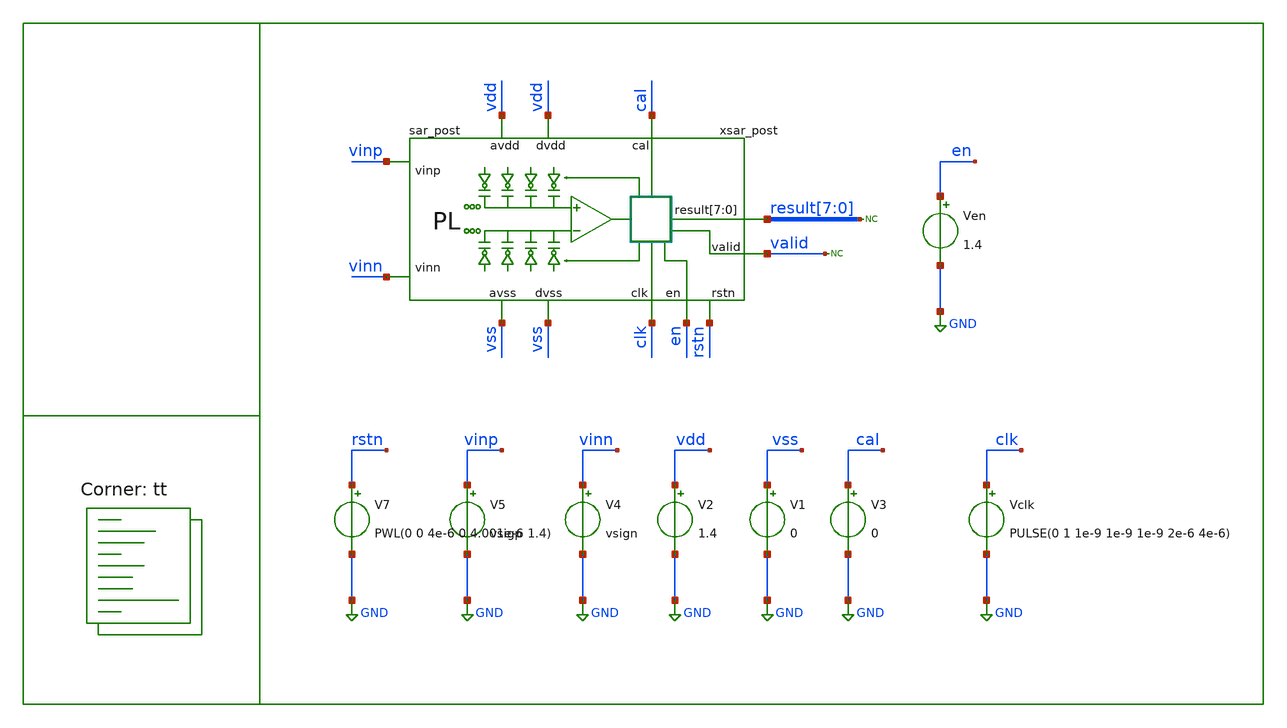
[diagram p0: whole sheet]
** sch_path: full_ext_sim/full_ext_sim.sch

.include /home/alex/Desktop/EDA/SAR_IPN/full_ext_sim/sar/comparator/comparator.spice
.include /home/alex/Desktop/EDA/SAR_IPN/full_ext_sim/sar/latch/latch.spice
.include /home/alex/Desktop/EDA/SAR_IPN/full_ext_sim/sar/dac/DAC.spice
*.include /home/alex/Desktop/EDA/SAR_IPN/full_ext_sim/sar/sarlogic/sar_logic_light.spice
.include /home/alex/Desktop/EDA/SAR_IPN/full_ext_sim/sar/sarlogic/sar_logic_full.spice
.include $::SKYWATER_STDCELLS/sky130_fd_sc_hd.spice
.include $::SKYWATER_STDCELLS/sky130_ef_sc_hd__decap_12.spice

.lib $::SKYWATER_MODELS/sky130.lib.spice tt
**.subckt full_ext_sim
V1 vss GND 0
V2 vdd GND 1.4
V4 vinn GND vsign
V5 vinp GND vsigp
Vclk clk GND PULSE(0 1 1e-9 1e-9 1e-9 2e-6 4e-6)
Ven en GND 1.4
* noconn valid
V3 cal GND 0
* noconn result[7:0]
xsar_post vdd vdd vss result[7] result[6] result[5] result[4] result[3] result[2] result[1]
+ result[0] vinn vss clk vinp en valid cal rstn sar_post
V7 rstn GND PWL(0 0 4e-6 0 4.001e-6 1.4)
**.ends

* expanding   symbol:  /home/alex/Desktop/EDA/SAR_IPN/full_ext_sim/sar/sar_post/sar_post.sym # of
*+ pins=12
** sym_path: full_extract_sim/sar/sar_post/sar_post.sym
** sch_path: full_extract_sim/sar/sar_post/sar_post.sch
.subckt sar_post avdd dvdd dvss result[7] result[6] result[5] result[4] result[3] result[2]
+ result[1] result[0] vinn avss clk vinp en valid cal rstn
*.iopin avss
*.iopin avdd
*.iopin dvss
*.iopin dvdd
*.ipin vinp
*.ipin vinn
*.opin result[7],result[6],result[5],result[4],result[3],result[2],result[1],result[0]
*.ipin clk
*.ipin en
*.opin valid
*.ipin cal
*.ipin rstn
xlat avdd avss net1 outp outn comp latch
* noconn #net1
* noconn comp
* noconn sample
* noconn ctln[7:0]
* noconn ctlp[7:0]
* noconn trim[4:0]
* noconn trimb[4:0]
* noconn result[7:0]
* noconn valid
* noconn clkc
* noconn clk
* noconn en
* noconn cal
xdn n_sample sample ctln[1] ctln[0] avss ctln[3] ctln[4] ctln[5] ctln[6] ctln[7] ctln[2] avdd avss
+ sample vn vinn DAC
xcom trim[3] trim[2] trim[0] trim[1] trim[4] trimb[4] trimb[1] trimb[0] trimb[2] trimb[3] outn outp
+ clkc avdd avss vn vp comparator
* noconn rstn
**** begin user architecture code


.model adc_buff adc_bridge(in_low = 0.2 in_high=0.8)
.model dac_buff dac_bridge(out_high = 1.2)

Aad [clk rstn en comp cal] [dclk drstn den dcomp dcal] adc_buff
Ada [dctlp0 dctlp1 dctlp2 dctlp3 dctlp4 dctlp5 dctlp6 dctlp7 dctln0 dctln1 dctln2 dctln3 dctln4
+ dctln5 dctln6 dctln7 dres0 dres1 dres2 dres3 dres4 dres5 dres6 dres7 dsamp dclkc] [ctlp_0_ ctlp_1_ ctlp_2_
+ ctlp_3_ ctlp_4_ ctlp_5_ ctlp_6_ ctlp_7_ ctln_0_ ctln_1_ ctln_2_ ctln_3_ ctln_4_ ctln_5_ ctln_6_ ctln_7_
+ res0 res1 res2 res3 res4 res5 res6 res7 sample clkc] dac_buff
Ada2 [dtrim4 dtrim3 dtrim2 dtrim1 dtrim0 dtrimb4 dtrimb3 dtrimb2 dtrimb1 dtrimb0] [trim_4_ trim_3_
+ trim_2_ trim_1_ trim_0_ trimb_4_ trimb_3_ trimb_2_ trimb_1_ trimb_0_ ] dac_buff
Xuut dclk drstn den dcomp dcal dvalid dres0 dres1 dres2 dres3 dres4 dres5 dres6 dres7 dsamp dctlp0
+ dctlp1 dctlp2 dctlp3 dctlp4 dctlp5 dctlp6 dctlp7 dctln0 dctln1 dctln2 dctln3 dctln4 dctln5 dctln6 dctln7
+ dtrim0 dtrim1 dtrim2 dtrim3 dtrim4 dtrimb0 dtrimb1 dtrimb2 dtrimb3 dtrimb4 dclkc sar_logic


**** end user architecture code
xdp n_sample sample ctlp[1] ctlp[0] avdd ctlp[3] ctlp[4] ctlp[5] ctlp[6] ctlp[7] ctlp[2] avdd avss
+ sample vp vinp DAC
x1 sample VGND VNB VPB VPWR n_sample sky130_fd_sc_hd__inv_1
.ends

.GLOBAL GND
**** begin user architecture code

.options method trap
*.options method gear
.options gmin 1e-15
.options abstol 1e-15
.options reltol 0.0001
.options vntol 0.1e-6
.options warn 1

.param MC_SWITCH=0
.param vin=0.1
.param vcm=0.7
.param vsigp={vcm + vin/2}
.param vsign={vcm - vin/2}

.tran 100e-9 48e-6
.save all
.control

run
*write full_ext_sim_light.raw
write full_ext_sim_full.raw
*meas tran d0 find v(xsar_post.res0) at=47e-6
*meas tran d1 find v(xsar_post.res1) at=47e-6
*meas tran d2 find v(xsar_post.res2) at=47e-6
*meas tran d3 find v(xsar_post.res3) at=47e-6
*meas tran d4 find v(xsar_post.res4) at=47e-6
*meas tran d5 find v(xsar_post.res5) at=47e-6
*meas tran d6 find v(xsar_post.res6) at=47e-6
*meas tran d7 find v(xsar_post.res7) at=47e-6

meas tran d0 find v(xsar.result_0_) at=47e-6
meas tran d1 find v(xsar.result_1_) at=47e-6
meas tran d2 find v(xsar.result_2_) at=47e-6
meas tran d3 find v(xsar.result_3_) at=47e-6
meas tran d4 find v(xsar.result_4_) at=47e-6
meas tran d5 find v(xsar.result_5_) at=47e-6
meas tran d6 find v(xsar.result_6_) at=47e-6
meas tran d7 find v(xsar.result_7_) at=47e-6

meas tran vpmax max xsar_post.vp
meas tran vpmin min xsar_post.vp
meas tran vpend find v(xsar_post.vp) at=39e-6

meas tran vnmax max xsar_post.vn
meas tran vnmin min xsar_post.vn
meas tran vnend find v(xsar_post.vn) at=39e-6

print d0
print d1
print d2
print d3
print d4
print d5
print d6
print d7

print vpmax
print vpmin

print vnmax
print vnmin

print vpend
print vnend

.endc


**** end user architecture code
.end
